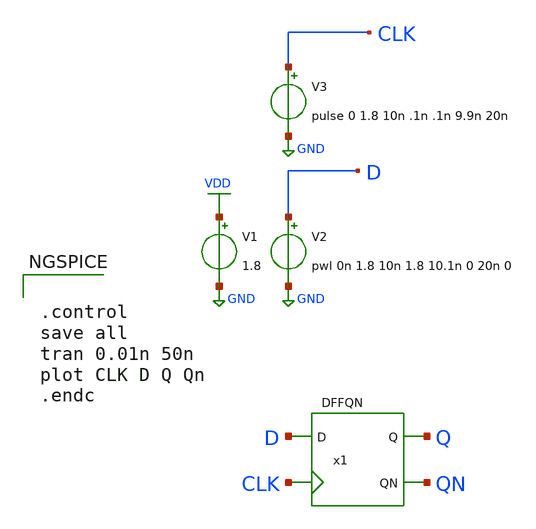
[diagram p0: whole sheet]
** sch_path: lib/xschem/test_DFFQN.sch
**.subckt test_DFFQN
V2 D GND pwl 0n 1.8 10n 1.8 10.1n 0 20n 0
V1 VDD GND 1.8
V3 CLK GND pulse 0 1.8 10n .1n .1n 9.9n 20n
x1 CLK Q D QN VDD GND DFFQN
**** begin user architecture code

.lib $::SKYWATER_MODELS/sky130.lib.spice tt


**** end user architecture code
**.ends

* expanding   symbol:  DFFQN.sym # of pins=4
** sym_path: lib/xschem/DFFQN.sym
** sch_path: lib/xschem/DFFQN.sch
.subckt DFFQN CLK Q D QN VCCPIN VSSPIN
*.ipin CLK
*.ipin D
*.opin Q
*.opin QN
XM8 net2 CLK_NOT net3 VSSPIN sky130_fd_pr__nfet_01v8 L=0.15 W=2 nf=1 ad='int((nf+1)/2) * W/nf * 0.29'
+ as='int((nf+2)/2) * W/nf * 0.29' pd='2*int((nf+1)/2) * (W/nf + 0.29)' ps='2*int((nf+2)/2) * (W/nf + 0.29)'
+ nrd='0.29 / W' nrs='0.29 / W' sa=0 sb=0 sd=0 mult=1 m=1
XM6 net1 D VCCPIN VCCPIN sky130_fd_pr__pfet_01v8 L=0.15 W=3 nf=1 ad='int((nf+1)/2) * W/nf * 0.29' as='int((nf+2)/2) * W/nf * 0.29'
+ pd='2*int((nf+1)/2) * (W/nf + 0.29)' ps='2*int((nf+2)/2) * (W/nf + 0.29)' nrd='0.29 / W' nrs='0.29 / W'
+ sa=0 sb=0 sd=0 mult=1 m=1
XM9 net3 D VSSPIN VSSPIN sky130_fd_pr__nfet_01v8 L=0.15 W=2 nf=1 ad='int((nf+1)/2) * W/nf * 0.29' as='int((nf+2)/2) * W/nf * 0.29'
+ pd='2*int((nf+1)/2) * (W/nf + 0.29)' ps='2*int((nf+2)/2) * (W/nf + 0.29)' nrd='0.29 / W' nrs='0.29 / W'
+ sa=0 sb=0 sd=0 mult=1 m=1
XM4 net2 CLK net1 VCCPIN sky130_fd_pr__pfet_01v8 L=0.15 W=3 nf=1 ad='int((nf+1)/2) * W/nf * 0.29' as='int((nf+2)/2) * W/nf * 0.29'
+ pd='2*int((nf+1)/2) * (W/nf + 0.29)' ps='2*int((nf+2)/2) * (W/nf + 0.29)' nrd='0.29 / W' nrs='0.29 / W'
+ sa=0 sb=0 sd=0 mult=1 m=1
XM5 net1 D VCCPIN VCCPIN sky130_fd_pr__pfet_01v8 L=0.15 W=3 nf=1 ad='int((nf+1)/2) * W/nf * 0.29' as='int((nf+2)/2) * W/nf * 0.29'
+ pd='2*int((nf+1)/2) * (W/nf + 0.29)' ps='2*int((nf+2)/2) * (W/nf + 0.29)' nrd='0.29 / W' nrs='0.29 / W'
+ sa=0 sb=0 sd=0 mult=1 m=1
XM7 net2 CLK net1 VCCPIN sky130_fd_pr__pfet_01v8 L=0.15 W=3 nf=1 ad='int((nf+1)/2) * W/nf * 0.29' as='int((nf+2)/2) * W/nf * 0.29'
+ pd='2*int((nf+1)/2) * (W/nf + 0.29)' ps='2*int((nf+2)/2) * (W/nf + 0.29)' nrd='0.29 / W' nrs='0.29 / W'
+ sa=0 sb=0 sd=0 mult=1 m=1
XM11 net5 CLK net6 VSSPIN sky130_fd_pr__nfet_01v8 L=0.15 W=2 nf=1 ad='int((nf+1)/2) * W/nf * 0.29' as='int((nf+2)/2) * W/nf * 0.29'
+ pd='2*int((nf+1)/2) * (W/nf + 0.29)' ps='2*int((nf+2)/2) * (W/nf + 0.29)' nrd='0.29 / W' nrs='0.29 / W'
+ sa=0 sb=0 sd=0 mult=1 m=1
XM12 net6 net7 VSSPIN VSSPIN sky130_fd_pr__nfet_01v8 L=0.15 W=2 nf=1 ad='int((nf+1)/2) * W/nf * 0.29'
+ as='int((nf+2)/2) * W/nf * 0.29' pd='2*int((nf+1)/2) * (W/nf + 0.29)' ps='2*int((nf+2)/2) * (W/nf + 0.29)'
+ nrd='0.29 / W' nrs='0.29 / W' sa=0 sb=0 sd=0 mult=1 m=1
XM1 net4 net7 VCCPIN VCCPIN sky130_fd_pr__pfet_01v8 L=0.15 W=3 nf=1 ad='int((nf+1)/2) * W/nf * 0.29'
+ as='int((nf+2)/2) * W/nf * 0.29' pd='2*int((nf+1)/2) * (W/nf + 0.29)' ps='2*int((nf+2)/2) * (W/nf + 0.29)'
+ nrd='0.29 / W' nrs='0.29 / W' sa=0 sb=0 sd=0 mult=1 m=1
XM2 net4 net7 VCCPIN VCCPIN sky130_fd_pr__pfet_01v8 L=0.15 W=3 nf=1 ad='int((nf+1)/2) * W/nf * 0.29'
+ as='int((nf+2)/2) * W/nf * 0.29' pd='2*int((nf+1)/2) * (W/nf + 0.29)' ps='2*int((nf+2)/2) * (W/nf + 0.29)'
+ nrd='0.29 / W' nrs='0.29 / W' sa=0 sb=0 sd=0 mult=1 m=1
XM3 net5 CLK_NOT net4 VCCPIN sky130_fd_pr__pfet_01v8 L=0.15 W=3 nf=1 ad='int((nf+1)/2) * W/nf * 0.29'
+ as='int((nf+2)/2) * W/nf * 0.29' pd='2*int((nf+1)/2) * (W/nf + 0.29)' ps='2*int((nf+2)/2) * (W/nf + 0.29)'
+ nrd='0.29 / W' nrs='0.29 / W' sa=0 sb=0 sd=0 mult=1 m=1
XM10 net5 CLK_NOT net4 VCCPIN sky130_fd_pr__pfet_01v8 L=0.15 W=3 nf=1 ad='int((nf+1)/2) * W/nf * 0.29'
+ as='int((nf+2)/2) * W/nf * 0.29' pd='2*int((nf+1)/2) * (W/nf + 0.29)' ps='2*int((nf+2)/2) * (W/nf + 0.29)'
+ nrd='0.29 / W' nrs='0.29 / W' sa=0 sb=0 sd=0 mult=1 m=1
XM19 net12 net7 VCCPIN VCCPIN sky130_fd_pr__pfet_01v8 L=0.15 W=3 nf=1 ad='int((nf+1)/2) * W/nf * 0.29'
+ as='int((nf+2)/2) * W/nf * 0.29' pd='2*int((nf+1)/2) * (W/nf + 0.29)' ps='2*int((nf+2)/2) * (W/nf + 0.29)'
+ nrd='0.29 / W' nrs='0.29 / W' sa=0 sb=0 sd=0 mult=1 m=1
XM20 net12 net7 VCCPIN VCCPIN sky130_fd_pr__pfet_01v8 L=0.15 W=3 nf=1 ad='int((nf+1)/2) * W/nf * 0.29'
+ as='int((nf+2)/2) * W/nf * 0.29' pd='2*int((nf+1)/2) * (W/nf + 0.29)' ps='2*int((nf+2)/2) * (W/nf + 0.29)'
+ nrd='0.29 / W' nrs='0.29 / W' sa=0 sb=0 sd=0 mult=1 m=1
XM21 net9 CLK_NOT net12 VCCPIN sky130_fd_pr__pfet_01v8 L=0.15 W=3 nf=1 ad='int((nf+1)/2) * W/nf * 0.29'
+ as='int((nf+2)/2) * W/nf * 0.29' pd='2*int((nf+1)/2) * (W/nf + 0.29)' ps='2*int((nf+2)/2) * (W/nf + 0.29)'
+ nrd='0.29 / W' nrs='0.29 / W' sa=0 sb=0 sd=0 mult=1 m=1
XM22 net9 CLK_NOT net12 VCCPIN sky130_fd_pr__pfet_01v8 L=0.15 W=3 nf=1 ad='int((nf+1)/2) * W/nf * 0.29'
+ as='int((nf+2)/2) * W/nf * 0.29' pd='2*int((nf+1)/2) * (W/nf + 0.29)' ps='2*int((nf+2)/2) * (W/nf + 0.29)'
+ nrd='0.29 / W' nrs='0.29 / W' sa=0 sb=0 sd=0 mult=1 m=1
XM23 net9 CLK net13 VSSPIN sky130_fd_pr__nfet_01v8 L=0.15 W=2 nf=1 ad='int((nf+1)/2) * W/nf * 0.29' as='int((nf+2)/2) * W/nf * 0.29'
+ pd='2*int((nf+1)/2) * (W/nf + 0.29)' ps='2*int((nf+2)/2) * (W/nf + 0.29)' nrd='0.29 / W' nrs='0.29 / W'
+ sa=0 sb=0 sd=0 mult=1 m=1
XM24 net13 net7 VSSPIN VSSPIN sky130_fd_pr__nfet_01v8 L=0.15 W=2 nf=1 ad='int((nf+1)/2) * W/nf * 0.29'
+ as='int((nf+2)/2) * W/nf * 0.29' pd='2*int((nf+1)/2) * (W/nf + 0.29)' ps='2*int((nf+2)/2) * (W/nf + 0.29)'
+ nrd='0.29 / W' nrs='0.29 / W' sa=0 sb=0 sd=0 mult=1 m=1
XM13 net8 net11 VCCPIN VCCPIN sky130_fd_pr__pfet_01v8 L=0.15 W=3 nf=1 ad='int((nf+1)/2) * W/nf * 0.29'
+ as='int((nf+2)/2) * W/nf * 0.29' pd='2*int((nf+1)/2) * (W/nf + 0.29)' ps='2*int((nf+2)/2) * (W/nf + 0.29)'
+ nrd='0.29 / W' nrs='0.29 / W' sa=0 sb=0 sd=0 mult=1 m=1
XM14 net8 net11 VCCPIN VCCPIN sky130_fd_pr__pfet_01v8 L=0.15 W=3 nf=1 ad='int((nf+1)/2) * W/nf * 0.29'
+ as='int((nf+2)/2) * W/nf * 0.29' pd='2*int((nf+1)/2) * (W/nf + 0.29)' ps='2*int((nf+2)/2) * (W/nf + 0.29)'
+ nrd='0.29 / W' nrs='0.29 / W' sa=0 sb=0 sd=0 mult=1 m=1
XM15 net9 CLK net8 VCCPIN sky130_fd_pr__pfet_01v8 L=0.15 W=3 nf=1 ad='int((nf+1)/2) * W/nf * 0.29' as='int((nf+2)/2) * W/nf * 0.29'
+ pd='2*int((nf+1)/2) * (W/nf + 0.29)' ps='2*int((nf+2)/2) * (W/nf + 0.29)' nrd='0.29 / W' nrs='0.29 / W'
+ sa=0 sb=0 sd=0 mult=1 m=1
XM16 net9 CLK net8 VCCPIN sky130_fd_pr__pfet_01v8 L=0.15 W=3 nf=1 ad='int((nf+1)/2) * W/nf * 0.29' as='int((nf+2)/2) * W/nf * 0.29'
+ pd='2*int((nf+1)/2) * (W/nf + 0.29)' ps='2*int((nf+2)/2) * (W/nf + 0.29)' nrd='0.29 / W' nrs='0.29 / W'
+ sa=0 sb=0 sd=0 mult=1 m=1
XM17 net9 CLK_NOT net10 VSSPIN sky130_fd_pr__nfet_01v8 L=0.15 W=2 nf=1 ad='int((nf+1)/2) * W/nf * 0.29'
+ as='int((nf+2)/2) * W/nf * 0.29' pd='2*int((nf+1)/2) * (W/nf + 0.29)' ps='2*int((nf+2)/2) * (W/nf + 0.29)'
+ nrd='0.29 / W' nrs='0.29 / W' sa=0 sb=0 sd=0 mult=1 m=1
XM18 net10 net11 VSSPIN VSSPIN sky130_fd_pr__nfet_01v8 L=0.15 W=2 nf=1 ad='int((nf+1)/2) * W/nf * 0.29'
+ as='int((nf+2)/2) * W/nf * 0.29' pd='2*int((nf+1)/2) * (W/nf + 0.29)' ps='2*int((nf+2)/2) * (W/nf + 0.29)'
+ nrd='0.29 / W' nrs='0.29 / W' sa=0 sb=0 sd=0 mult=1 m=1
x1 CLK_NOT CLK VCCPIN VSSPIN INVX1
x2 net7 net2 VCCPIN VSSPIN INVX1
x3 net11 net9 VCCPIN VSSPIN INVX1
x4 QN net11 VCCPIN VSSPIN INVX1
x5 Q QN VCCPIN VSSPIN INVX1
.ends


* expanding   symbol:  INVX1.sym # of pins=2
** sym_path: lib/xschem/INVX1.sym
** sch_path: lib/xschem/INVX1.sch
.subckt INVX1 Y A VCCPIN VSSPIN
*.ipin A
*.opin Y
XM1 Y A VSSPIN VSSPIN sky130_fd_pr__nfet_01v8 L=0.15 W=3 nf=1 ad='int((nf+1)/2) * W/nf * 0.29' as='int((nf+2)/2) * W/nf * 0.29'
+ pd='2*int((nf+1)/2) * (W/nf + 0.29)' ps='2*int((nf+2)/2) * (W/nf + 0.29)' nrd='0.29 / W' nrs='0.29 / W'
+ sa=0 sb=0 sd=0 mult=1 m=1
XM2 Y A VCCPIN VCCPIN sky130_fd_pr__pfet_01v8 L=0.15 W=2 nf=1 ad='int((nf+1)/2) * W/nf * 0.29' as='int((nf+2)/2) * W/nf * 0.29'
+ pd='2*int((nf+1)/2) * (W/nf + 0.29)' ps='2*int((nf+2)/2) * (W/nf + 0.29)' nrd='0.29 / W' nrs='0.29 / W'
+ sa=0 sb=0 sd=0 mult=1 m=1
XM3 Y A VCCPIN VCCPIN sky130_fd_pr__pfet_01v8 L=0.15 W=2 nf=1 ad='int((nf+1)/2) * W/nf * 0.29' as='int((nf+2)/2) * W/nf * 0.29'
+ pd='2*int((nf+1)/2) * (W/nf + 0.29)' ps='2*int((nf+2)/2) * (W/nf + 0.29)' nrd='0.29 / W' nrs='0.29 / W'
+ sa=0 sb=0 sd=0 mult=1 m=1
.ends

.GLOBAL VDD
.GLOBAL GND
**** begin user architecture code


.control
save all
tran 0.01n 50n
plot CLK D Q Qn
.endc


**** end user architecture code
.end
